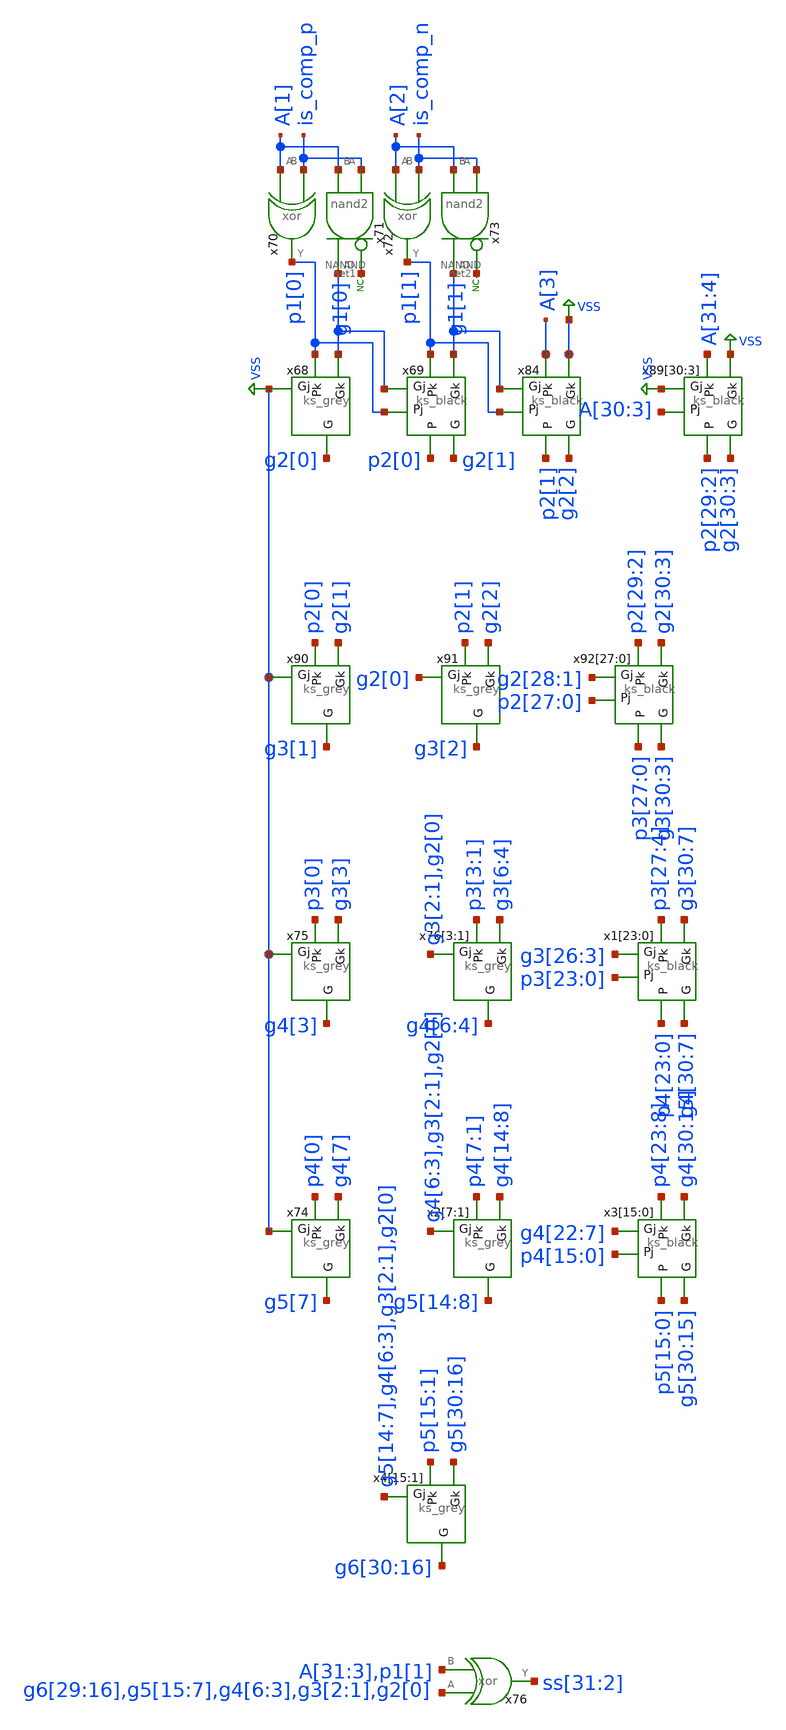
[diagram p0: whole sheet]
** sch_path: elements/add_vars.sch
**.subckt add_vars
x68 p1[0] VSS g1[0] g2[0] ks_grey
x69 p1[1] g1[0] g1[1] g2[1] p1[0] p2[0] ks_black
x70 A[1] is_comp_p p1[0] xor
x71 net1 g1[0] is_comp_p A[1] nand2
* noconn #net1
x72 A[2] is_comp_n p1[1] xor
x73 net2 g1[1] is_comp_n A[2] nand2
* noconn #net2
x84 A[3] g1[1] VSS g2[2] p1[1] p2[1] ks_black
x89[30] A[31] VSS VSS g2[30] A[30] p2[29] ks_black
x89[29] A[30] VSS VSS g2[29] A[29] p2[28] ks_black
x89[28] A[29] VSS VSS g2[28] A[28] p2[27] ks_black
x89[27] A[28] VSS VSS g2[27] A[27] p2[26] ks_black
x89[26] A[27] VSS VSS g2[26] A[26] p2[25] ks_black
x89[25] A[26] VSS VSS g2[25] A[25] p2[24] ks_black
x89[24] A[25] VSS VSS g2[24] A[24] p2[23] ks_black
x89[23] A[24] VSS VSS g2[23] A[23] p2[22] ks_black
x89[22] A[23] VSS VSS g2[22] A[22] p2[21] ks_black
x89[21] A[22] VSS VSS g2[21] A[21] p2[20] ks_black
x89[20] A[21] VSS VSS g2[20] A[20] p2[19] ks_black
x89[19] A[20] VSS VSS g2[19] A[19] p2[18] ks_black
x89[18] A[19] VSS VSS g2[18] A[18] p2[17] ks_black
x89[17] A[18] VSS VSS g2[17] A[17] p2[16] ks_black
x89[16] A[17] VSS VSS g2[16] A[16] p2[15] ks_black
x89[15] A[16] VSS VSS g2[15] A[15] p2[14] ks_black
x89[14] A[15] VSS VSS g2[14] A[14] p2[13] ks_black
x89[13] A[14] VSS VSS g2[13] A[13] p2[12] ks_black
x89[12] A[13] VSS VSS g2[12] A[12] p2[11] ks_black
x89[11] A[12] VSS VSS g2[11] A[11] p2[10] ks_black
x89[10] A[11] VSS VSS g2[10] A[10] p2[9] ks_black
x89[9] A[10] VSS VSS g2[9] A[9] p2[8] ks_black
x89[8] A[9] VSS VSS g2[8] A[8] p2[7] ks_black
x89[7] A[8] VSS VSS g2[7] A[7] p2[6] ks_black
x89[6] A[7] VSS VSS g2[6] A[6] p2[5] ks_black
x89[5] A[6] VSS VSS g2[5] A[5] p2[4] ks_black
x89[4] A[5] VSS VSS g2[4] A[4] p2[3] ks_black
x89[3] A[4] VSS VSS g2[3] A[3] p2[2] ks_black
x90 p2[0] VSS g2[1] g3[1] ks_grey
x91 p2[1] g2[0] g2[2] g3[2] ks_grey
x92[27] p2[29] g2[28] g2[30] g3[30] p2[27] p3[27] ks_black
x92[26] p2[28] g2[27] g2[29] g3[29] p2[26] p3[26] ks_black
x92[25] p2[27] g2[26] g2[28] g3[28] p2[25] p3[25] ks_black
x92[24] p2[26] g2[25] g2[27] g3[27] p2[24] p3[24] ks_black
x92[23] p2[25] g2[24] g2[26] g3[26] p2[23] p3[23] ks_black
x92[22] p2[24] g2[23] g2[25] g3[25] p2[22] p3[22] ks_black
x92[21] p2[23] g2[22] g2[24] g3[24] p2[21] p3[21] ks_black
x92[20] p2[22] g2[21] g2[23] g3[23] p2[20] p3[20] ks_black
x92[19] p2[21] g2[20] g2[22] g3[22] p2[19] p3[19] ks_black
x92[18] p2[20] g2[19] g2[21] g3[21] p2[18] p3[18] ks_black
x92[17] p2[19] g2[18] g2[20] g3[20] p2[17] p3[17] ks_black
x92[16] p2[18] g2[17] g2[19] g3[19] p2[16] p3[16] ks_black
x92[15] p2[17] g2[16] g2[18] g3[18] p2[15] p3[15] ks_black
x92[14] p2[16] g2[15] g2[17] g3[17] p2[14] p3[14] ks_black
x92[13] p2[15] g2[14] g2[16] g3[16] p2[13] p3[13] ks_black
x92[12] p2[14] g2[13] g2[15] g3[15] p2[12] p3[12] ks_black
x92[11] p2[13] g2[12] g2[14] g3[14] p2[11] p3[11] ks_black
x92[10] p2[12] g2[11] g2[13] g3[13] p2[10] p3[10] ks_black
x92[9] p2[11] g2[10] g2[12] g3[12] p2[9] p3[9] ks_black
x92[8] p2[10] g2[9] g2[11] g3[11] p2[8] p3[8] ks_black
x92[7] p2[9] g2[8] g2[10] g3[10] p2[7] p3[7] ks_black
x92[6] p2[8] g2[7] g2[9] g3[9] p2[6] p3[6] ks_black
x92[5] p2[7] g2[6] g2[8] g3[8] p2[5] p3[5] ks_black
x92[4] p2[6] g2[5] g2[7] g3[7] p2[4] p3[4] ks_black
x92[3] p2[5] g2[4] g2[6] g3[6] p2[3] p3[3] ks_black
x92[2] p2[4] g2[3] g2[5] g3[5] p2[2] p3[2] ks_black
x92[1] p2[3] g2[2] g2[4] g3[4] p2[1] p3[1] ks_black
x92[0] p2[2] g2[1] g2[3] g3[3] p2[0] p3[0] ks_black
x75 p3[0] VSS g3[3] g4[3] ks_grey
x76[3] p3[3] g3[2] g3[6] g4[6] ks_grey
x76[2] p3[2] g3[1] g3[5] g4[5] ks_grey
x76[1] p3[1] g2[0] g3[4] g4[4] ks_grey
x1[23] p3[27] g3[26] g3[30] g4[30] p3[23] p4[23] ks_black
x1[22] p3[26] g3[25] g3[29] g4[29] p3[22] p4[22] ks_black
x1[21] p3[25] g3[24] g3[28] g4[28] p3[21] p4[21] ks_black
x1[20] p3[24] g3[23] g3[27] g4[27] p3[20] p4[20] ks_black
x1[19] p3[23] g3[22] g3[26] g4[26] p3[19] p4[19] ks_black
x1[18] p3[22] g3[21] g3[25] g4[25] p3[18] p4[18] ks_black
x1[17] p3[21] g3[20] g3[24] g4[24] p3[17] p4[17] ks_black
x1[16] p3[20] g3[19] g3[23] g4[23] p3[16] p4[16] ks_black
x1[15] p3[19] g3[18] g3[22] g4[22] p3[15] p4[15] ks_black
x1[14] p3[18] g3[17] g3[21] g4[21] p3[14] p4[14] ks_black
x1[13] p3[17] g3[16] g3[20] g4[20] p3[13] p4[13] ks_black
x1[12] p3[16] g3[15] g3[19] g4[19] p3[12] p4[12] ks_black
x1[11] p3[15] g3[14] g3[18] g4[18] p3[11] p4[11] ks_black
x1[10] p3[14] g3[13] g3[17] g4[17] p3[10] p4[10] ks_black
x1[9] p3[13] g3[12] g3[16] g4[16] p3[9] p4[9] ks_black
x1[8] p3[12] g3[11] g3[15] g4[15] p3[8] p4[8] ks_black
x1[7] p3[11] g3[10] g3[14] g4[14] p3[7] p4[7] ks_black
x1[6] p3[10] g3[9] g3[13] g4[13] p3[6] p4[6] ks_black
x1[5] p3[9] g3[8] g3[12] g4[12] p3[5] p4[5] ks_black
x1[4] p3[8] g3[7] g3[11] g4[11] p3[4] p4[4] ks_black
x1[3] p3[7] g3[6] g3[10] g4[10] p3[3] p4[3] ks_black
x1[2] p3[6] g3[5] g3[9] g4[9] p3[2] p4[2] ks_black
x1[1] p3[5] g3[4] g3[8] g4[8] p3[1] p4[1] ks_black
x1[0] p3[4] g3[3] g3[7] g4[7] p3[0] p4[0] ks_black
x74 p4[0] VSS g4[7] g5[7] ks_grey
x2[7] p4[7] g4[6] g4[14] g5[14] ks_grey
x2[6] p4[6] g4[5] g4[13] g5[13] ks_grey
x2[5] p4[5] g4[4] g4[12] g5[12] ks_grey
x2[4] p4[4] g4[3] g4[11] g5[11] ks_grey
x2[3] p4[3] g3[2] g4[10] g5[10] ks_grey
x2[2] p4[2] g3[1] g4[9] g5[9] ks_grey
x2[1] p4[1] g2[0] g4[8] g5[8] ks_grey
x3[15] p4[23] g4[22] g4[30] g5[30] p4[15] p5[15] ks_black
x3[14] p4[22] g4[21] g4[29] g5[29] p4[14] p5[14] ks_black
x3[13] p4[21] g4[20] g4[28] g5[28] p4[13] p5[13] ks_black
x3[12] p4[20] g4[19] g4[27] g5[27] p4[12] p5[12] ks_black
x3[11] p4[19] g4[18] g4[26] g5[26] p4[11] p5[11] ks_black
x3[10] p4[18] g4[17] g4[25] g5[25] p4[10] p5[10] ks_black
x3[9] p4[17] g4[16] g4[24] g5[24] p4[9] p5[9] ks_black
x3[8] p4[16] g4[15] g4[23] g5[23] p4[8] p5[8] ks_black
x3[7] p4[15] g4[14] g4[22] g5[22] p4[7] p5[7] ks_black
x3[6] p4[14] g4[13] g4[21] g5[21] p4[6] p5[6] ks_black
x3[5] p4[13] g4[12] g4[20] g5[20] p4[5] p5[5] ks_black
x3[4] p4[12] g4[11] g4[19] g5[19] p4[4] p5[4] ks_black
x3[3] p4[11] g4[10] g4[18] g5[18] p4[3] p5[3] ks_black
x3[2] p4[10] g4[9] g4[17] g5[17] p4[2] p5[2] ks_black
x3[1] p4[9] g4[8] g4[16] g5[16] p4[1] p5[1] ks_black
x3[0] p4[8] g4[7] g4[15] g5[15] p4[0] p5[0] ks_black
x4[15] p5[15] g5[14] g5[30] g6[30] ks_grey
x4[14] p5[14] g5[13] g5[29] g6[29] ks_grey
x4[13] p5[13] g5[12] g5[28] g6[28] ks_grey
x4[12] p5[12] g5[11] g5[27] g6[27] ks_grey
x4[11] p5[11] g5[10] g5[26] g6[26] ks_grey
x4[10] p5[10] g5[9] g5[25] g6[25] ks_grey
x4[9] p5[9] g5[8] g5[24] g6[24] ks_grey
x4[8] p5[8] g5[7] g5[23] g6[23] ks_grey
x4[7] p5[7] g4[6] g5[22] g6[22] ks_grey
x4[6] p5[6] g4[5] g5[21] g6[21] ks_grey
x4[5] p5[5] g4[4] g5[20] g6[20] ks_grey
x4[4] p5[4] g4[3] g5[19] g6[19] ks_grey
x4[3] p5[3] g3[2] g5[18] g6[18] ks_grey
x4[2] p5[2] g3[1] g5[17] g6[17] ks_grey
x4[1] p5[1] g2[0] g5[16] g6[16] ks_grey
x76 g6[29] A[31] ss[31] xor
**.ends
.GLOBAL VSS
.end
